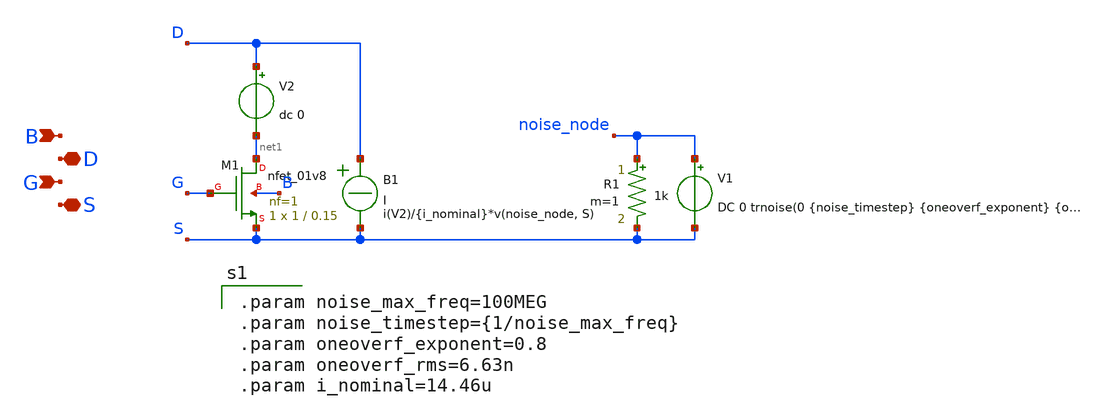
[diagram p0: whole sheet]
** sch_path: nmos_noisy.sch
**.subckt nmos_noisy S G D B
*.iopin S
*.ipin G
*.iopin D
*.ipin B
XM1 net1 G S B sky130_fd_pr__nfet_01v8 L=0.15 W=1 nf=1 ad='int((nf+1)/2) * W/nf * 0.29' as='int((nf+2)/2) * W/nf * 0.29'
+ pd='2*int((nf+1)/2) * (W/nf + 0.29)' ps='2*int((nf+2)/2) * (W/nf + 0.29)' nrd='0.29 / W' nrs='0.29 / W'
+ sa=0 sb=0 sd=0 mult=1 m=1
V1 noise_node S DC 0 trnoise(0 {noise_timestep} {oneoverf_exponent} {oneoverf_rms})
B1 D S I = i(V2)/{i_nominal}*v(noise_node, S)
V2 D net1 dc 0
R1 noise_node S 1k m=1
**** begin user architecture code

.param noise_max_freq=100MEG
.param noise_timestep={1/noise_max_freq}
.param oneoverf_exponent=0.8
.param oneoverf_rms=6.63n
.param i_nominal=14.46u

**** end user architecture code
**.ends
.end
